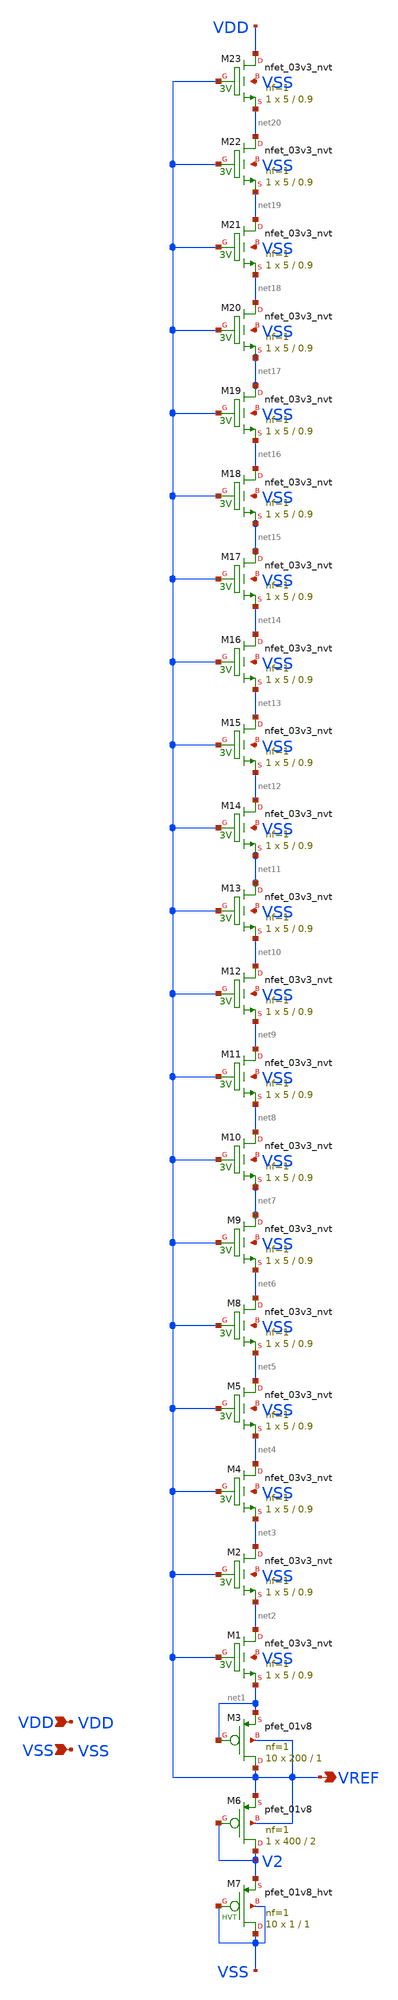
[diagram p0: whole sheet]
** sch_path: design/LELO_SVOD_SKY130A/LELO_SVOD_VTREF.sch
**.subckt LELO_SVOD_VTREF VDD VSS VREF
*.ipin VDD
*.ipin VSS
*.opin VREF
XM1 net2 VREF net1 VSS sky130_fd_pr__nfet_03v3_nvt L=0.9 W=5 nf=1 ad='int((1 + 1)/2) * 5 / 1 * 0.29'
+ as='int((1 + 2)/2) * 5 / 1 * 0.29' pd='2*int((1 + 1)/2) * (5 / 1 + 0.29)' ps='2*int((1 + 2)/2) * (5 / 1 + 0.29)'
+ nrd='0.29 / 5 ' nrs='0.29 / 5 ' sa=0 sb=0 sd=0 mult=1 m=1
XM2 net3 VREF net2 VSS sky130_fd_pr__nfet_03v3_nvt L=0.9 W=5 nf=1 ad='int((1 + 1)/2) * 5 / 1 * 0.29'
+ as='int((1 + 2)/2) * 5 / 1 * 0.29' pd='2*int((1 + 1)/2) * (5 / 1 + 0.29)' ps='2*int((1 + 2)/2) * (5 / 1 + 0.29)'
+ nrd='0.29 / 5 ' nrs='0.29 / 5 ' sa=0 sb=0 sd=0 mult=1 m=1
XM3 VREF net1 net1 VREF sky130_fd_pr__pfet_01v8 L=1 W=200 nf=1 ad='int((1 + 1)/2) * 200 / 1 * 0.29' as='int((1 + 2)/2) * 200 / 1 * 0.29'
+ pd='2*int((1 + 1)/2) * (200 / 1 + 0.29)' ps='2*int((1 + 2)/2) * (200 / 1 + 0.29)' nrd='0.29 / 200 ' nrs='0.29 / 200 '
+ sa=0 sb=0 sd=0 mult=10 m=10
XM4 net4 VREF net3 VSS sky130_fd_pr__nfet_03v3_nvt L=0.9 W=5 nf=1 ad='int((1 + 1)/2) * 5 / 1 * 0.29'
+ as='int((1 + 2)/2) * 5 / 1 * 0.29' pd='2*int((1 + 1)/2) * (5 / 1 + 0.29)' ps='2*int((1 + 2)/2) * (5 / 1 + 0.29)'
+ nrd='0.29 / 5 ' nrs='0.29 / 5 ' sa=0 sb=0 sd=0 mult=1 m=1
XM5 net5 VREF net4 VSS sky130_fd_pr__nfet_03v3_nvt L=0.9 W=5 nf=1 ad='int((1 + 1)/2) * 5 / 1 * 0.29'
+ as='int((1 + 2)/2) * 5 / 1 * 0.29' pd='2*int((1 + 1)/2) * (5 / 1 + 0.29)' ps='2*int((1 + 2)/2) * (5 / 1 + 0.29)'
+ nrd='0.29 / 5 ' nrs='0.29 / 5 ' sa=0 sb=0 sd=0 mult=1 m=1
XM6 V2 V2 VREF VREF sky130_fd_pr__pfet_01v8 L=2 W=400 nf=1 ad='int((1 + 1)/2) * 400 / 1 * 0.29' as='int((1 + 2)/2) * 400 / 1 * 0.29'
+ pd='2*int((1 + 1)/2) * (400 / 1 + 0.29)' ps='2*int((1 + 2)/2) * (400 / 1 + 0.29)' nrd='0.29 / 400 ' nrs='0.29 / 400 '
+ sa=0 sb=0 sd=0 mult=1 m=1
XM7 VSS VSS V2 VSS sky130_fd_pr__pfet_01v8_hvt L=1 W=1 nf=1 ad='int((1 + 1)/2) * 1 / 1 * 0.29' as='int((1 + 2)/2) * 1 / 1 * 0.29'
+ pd='2*int((1 + 1)/2) * (1 / 1 + 0.29)' ps='2*int((1 + 2)/2) * (1 / 1 + 0.29)' nrd='0.29 / 1 ' nrs='0.29 / 1 '
+ sa=0 sb=0 sd=0 mult=10 m=10
XM8 net6 VREF net5 VSS sky130_fd_pr__nfet_03v3_nvt L=0.9 W=5 nf=1 ad='int((1 + 1)/2) * 5 / 1 * 0.29'
+ as='int((1 + 2)/2) * 5 / 1 * 0.29' pd='2*int((1 + 1)/2) * (5 / 1 + 0.29)' ps='2*int((1 + 2)/2) * (5 / 1 + 0.29)'
+ nrd='0.29 / 5 ' nrs='0.29 / 5 ' sa=0 sb=0 sd=0 mult=1 m=1
XM9 net7 VREF net6 VSS sky130_fd_pr__nfet_03v3_nvt L=0.9 W=5 nf=1 ad='int((1 + 1)/2) * 5 / 1 * 0.29'
+ as='int((1 + 2)/2) * 5 / 1 * 0.29' pd='2*int((1 + 1)/2) * (5 / 1 + 0.29)' ps='2*int((1 + 2)/2) * (5 / 1 + 0.29)'
+ nrd='0.29 / 5 ' nrs='0.29 / 5 ' sa=0 sb=0 sd=0 mult=1 m=1
XM10 net8 VREF net7 VSS sky130_fd_pr__nfet_03v3_nvt L=0.9 W=5 nf=1 ad='int((1 + 1)/2) * 5 / 1 * 0.29'
+ as='int((1 + 2)/2) * 5 / 1 * 0.29' pd='2*int((1 + 1)/2) * (5 / 1 + 0.29)' ps='2*int((1 + 2)/2) * (5 / 1 + 0.29)'
+ nrd='0.29 / 5 ' nrs='0.29 / 5 ' sa=0 sb=0 sd=0 mult=1 m=1
XM11 net9 VREF net8 VSS sky130_fd_pr__nfet_03v3_nvt L=0.9 W=5 nf=1 ad='int((1 + 1)/2) * 5 / 1 * 0.29'
+ as='int((1 + 2)/2) * 5 / 1 * 0.29' pd='2*int((1 + 1)/2) * (5 / 1 + 0.29)' ps='2*int((1 + 2)/2) * (5 / 1 + 0.29)'
+ nrd='0.29 / 5 ' nrs='0.29 / 5 ' sa=0 sb=0 sd=0 mult=1 m=1
XM12 net10 VREF net9 VSS sky130_fd_pr__nfet_03v3_nvt L=0.9 W=5 nf=1 ad='int((1 + 1)/2) * 5 / 1 * 0.29'
+ as='int((1 + 2)/2) * 5 / 1 * 0.29' pd='2*int((1 + 1)/2) * (5 / 1 + 0.29)' ps='2*int((1 + 2)/2) * (5 / 1 + 0.29)'
+ nrd='0.29 / 5 ' nrs='0.29 / 5 ' sa=0 sb=0 sd=0 mult=1 m=1
XM13 net11 VREF net10 VSS sky130_fd_pr__nfet_03v3_nvt L=0.9 W=5 nf=1 ad='int((1 + 1)/2) * 5 / 1 * 0.29'
+ as='int((1 + 2)/2) * 5 / 1 * 0.29' pd='2*int((1 + 1)/2) * (5 / 1 + 0.29)' ps='2*int((1 + 2)/2) * (5 / 1 + 0.29)'
+ nrd='0.29 / 5 ' nrs='0.29 / 5 ' sa=0 sb=0 sd=0 mult=1 m=1
XM14 net12 VREF net11 VSS sky130_fd_pr__nfet_03v3_nvt L=0.9 W=5 nf=1 ad='int((1 + 1)/2) * 5 / 1 * 0.29'
+ as='int((1 + 2)/2) * 5 / 1 * 0.29' pd='2*int((1 + 1)/2) * (5 / 1 + 0.29)' ps='2*int((1 + 2)/2) * (5 / 1 + 0.29)'
+ nrd='0.29 / 5 ' nrs='0.29 / 5 ' sa=0 sb=0 sd=0 mult=1 m=1
XM15 net13 VREF net12 VSS sky130_fd_pr__nfet_03v3_nvt L=0.9 W=5 nf=1 ad='int((1 + 1)/2) * 5 / 1 * 0.29'
+ as='int((1 + 2)/2) * 5 / 1 * 0.29' pd='2*int((1 + 1)/2) * (5 / 1 + 0.29)' ps='2*int((1 + 2)/2) * (5 / 1 + 0.29)'
+ nrd='0.29 / 5 ' nrs='0.29 / 5 ' sa=0 sb=0 sd=0 mult=1 m=1
XM16 net14 VREF net13 VSS sky130_fd_pr__nfet_03v3_nvt L=0.9 W=5 nf=1 ad='int((1 + 1)/2) * 5 / 1 * 0.29'
+ as='int((1 + 2)/2) * 5 / 1 * 0.29' pd='2*int((1 + 1)/2) * (5 / 1 + 0.29)' ps='2*int((1 + 2)/2) * (5 / 1 + 0.29)'
+ nrd='0.29 / 5 ' nrs='0.29 / 5 ' sa=0 sb=0 sd=0 mult=1 m=1
XM17 net15 VREF net14 VSS sky130_fd_pr__nfet_03v3_nvt L=0.9 W=5 nf=1 ad='int((1 + 1)/2) * 5 / 1 * 0.29'
+ as='int((1 + 2)/2) * 5 / 1 * 0.29' pd='2*int((1 + 1)/2) * (5 / 1 + 0.29)' ps='2*int((1 + 2)/2) * (5 / 1 + 0.29)'
+ nrd='0.29 / 5 ' nrs='0.29 / 5 ' sa=0 sb=0 sd=0 mult=1 m=1
XM18 net16 VREF net15 VSS sky130_fd_pr__nfet_03v3_nvt L=0.9 W=5 nf=1 ad='int((1 + 1)/2) * 5 / 1 * 0.29'
+ as='int((1 + 2)/2) * 5 / 1 * 0.29' pd='2*int((1 + 1)/2) * (5 / 1 + 0.29)' ps='2*int((1 + 2)/2) * (5 / 1 + 0.29)'
+ nrd='0.29 / 5 ' nrs='0.29 / 5 ' sa=0 sb=0 sd=0 mult=1 m=1
XM19 net17 VREF net16 VSS sky130_fd_pr__nfet_03v3_nvt L=0.9 W=5 nf=1 ad='int((1 + 1)/2) * 5 / 1 * 0.29'
+ as='int((1 + 2)/2) * 5 / 1 * 0.29' pd='2*int((1 + 1)/2) * (5 / 1 + 0.29)' ps='2*int((1 + 2)/2) * (5 / 1 + 0.29)'
+ nrd='0.29 / 5 ' nrs='0.29 / 5 ' sa=0 sb=0 sd=0 mult=1 m=1
XM20 net18 VREF net17 VSS sky130_fd_pr__nfet_03v3_nvt L=0.9 W=5 nf=1 ad='int((1 + 1)/2) * 5 / 1 * 0.29'
+ as='int((1 + 2)/2) * 5 / 1 * 0.29' pd='2*int((1 + 1)/2) * (5 / 1 + 0.29)' ps='2*int((1 + 2)/2) * (5 / 1 + 0.29)'
+ nrd='0.29 / 5 ' nrs='0.29 / 5 ' sa=0 sb=0 sd=0 mult=1 m=1
XM21 net19 VREF net18 VSS sky130_fd_pr__nfet_03v3_nvt L=0.9 W=5 nf=1 ad='int((1 + 1)/2) * 5 / 1 * 0.29'
+ as='int((1 + 2)/2) * 5 / 1 * 0.29' pd='2*int((1 + 1)/2) * (5 / 1 + 0.29)' ps='2*int((1 + 2)/2) * (5 / 1 + 0.29)'
+ nrd='0.29 / 5 ' nrs='0.29 / 5 ' sa=0 sb=0 sd=0 mult=1 m=1
XM22 net20 VREF net19 VSS sky130_fd_pr__nfet_03v3_nvt L=0.9 W=5 nf=1 ad='int((1 + 1)/2) * 5 / 1 * 0.29'
+ as='int((1 + 2)/2) * 5 / 1 * 0.29' pd='2*int((1 + 1)/2) * (5 / 1 + 0.29)' ps='2*int((1 + 2)/2) * (5 / 1 + 0.29)'
+ nrd='0.29 / 5 ' nrs='0.29 / 5 ' sa=0 sb=0 sd=0 mult=1 m=1
XM23 VDD VREF net20 VSS sky130_fd_pr__nfet_03v3_nvt L=0.9 W=5 nf=1 ad='int((1 + 1)/2) * 5 / 1 * 0.29'
+ as='int((1 + 2)/2) * 5 / 1 * 0.29' pd='2*int((1 + 1)/2) * (5 / 1 + 0.29)' ps='2*int((1 + 2)/2) * (5 / 1 + 0.29)'
+ nrd='0.29 / 5 ' nrs='0.29 / 5 ' sa=0 sb=0 sd=0 mult=1 m=1
**.ends
.end
